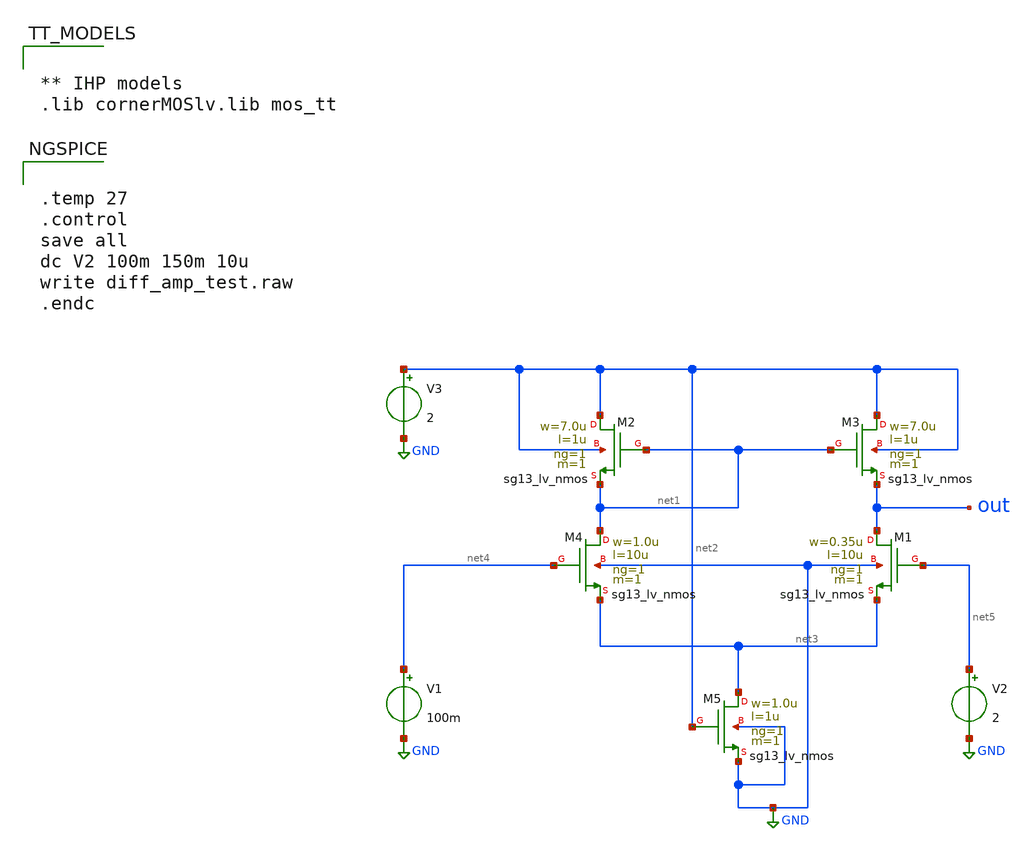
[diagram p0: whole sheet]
** sch_path: TempSensor/design_data/xschem/diff_amp_test.sch
**.subckt diff_amp_test
XM2 net2 net1 net1 net2 sg13_lv_nmos w=7.0u l=1u ng=1 m=1 mm_ok=1
XM1 out net5 net3 GND sg13_lv_nmos w=0.35u l=10u ng=1 m=1 mm_ok=1
XM3 net2 net1 out net2 sg13_lv_nmos w=7.0u l=1u ng=1 m=1 mm_ok=1
XM4 net1 net4 net3 GND sg13_lv_nmos w=1.0u l=10u ng=1 m=1 mm_ok=1
XM5 net3 net2 GND GND sg13_lv_nmos w=1.0u l=1u ng=1 m=1 mm_ok=1
V1 net4 GND 100m
V2 net5 GND 2
V3 net2 GND 2
**** begin user architecture code


.temp 27
.control
save all
dc V2 100m 150m 10u
write diff_amp_test.raw
.endc




** IHP models
.lib cornerMOSlv.lib mos_tt


**** end user architecture code
**.ends
.GLOBAL GND
.end
